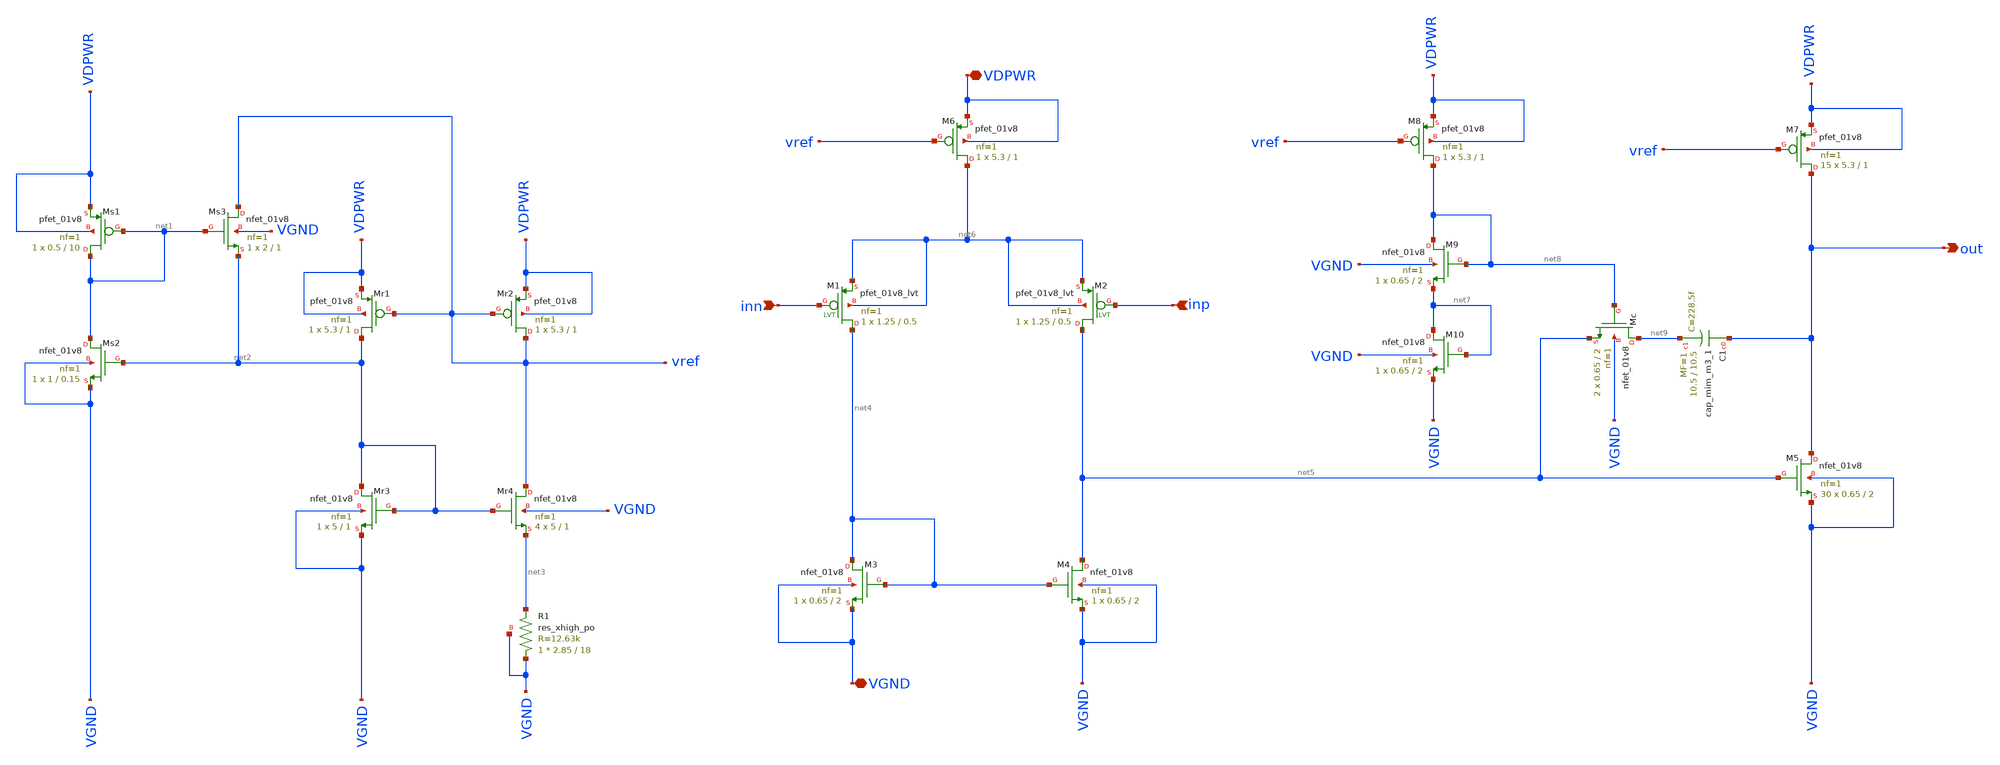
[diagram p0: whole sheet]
** sch_path: src/xschem/miller_ota.sch
**.subckt miller_ota inp out inn VDPWR VGND
*.ipin inp
*.opin out
*.ipin inn
*.iopin VDPWR
*.iopin VGND
XMs1 net1 net1 VDPWR VDPWR sky130_fd_pr__pfet_01v8 L=10 W=0.5 nf=1 ad='int((1 + 1)/2) * 0.5 / 1 * 0.29'
+ as='int((1 + 2)/2) * 0.5 / 1 * 0.29' pd='2*int((1 + 1)/2) * (0.5 / 1 + 0.29)' ps='2*int((1 + 2)/2) * (0.5 / 1 + 0.29)'
+ nrd='0.29 / 0.5 ' nrs='0.29 / 0.5 ' sa=0 sb=0 sd=0 mult=1 m=1
XMs3 vref net1 net2 VGND sky130_fd_pr__nfet_01v8 L=1 W=2 nf=1 ad='int((1 + 1)/2) * 2 / 1 * 0.29' as='int((1 + 2)/2) * 2 / 1 * 0.29'
+ pd='2*int((1 + 1)/2) * (2 / 1 + 0.29)' ps='2*int((1 + 2)/2) * (2 / 1 + 0.29)' nrd='0.29 / 2 ' nrs='0.29 / 2 '
+ sa=0 sb=0 sd=0 mult=1 m=1
XMs2 net1 net2 VGND VGND sky130_fd_pr__nfet_01v8 L=0.15 W=1 nf=1 ad='int((1 + 1)/2) * 1 / 1 * 0.29' as='int((1 + 2)/2) * 1 / 1 * 0.29'
+ pd='2*int((1 + 1)/2) * (1 / 1 + 0.29)' ps='2*int((1 + 2)/2) * (1 / 1 + 0.29)' nrd='0.29 / 1 ' nrs='0.29 / 1 '
+ sa=0 sb=0 sd=0 mult=1 m=1
XMr3 net2 net2 VGND VGND sky130_fd_pr__nfet_01v8 L=1 W=5 nf=1 ad='int((1 + 1)/2) * 5 / 1 * 0.29' as='int((1 + 2)/2) * 5 / 1 * 0.29'
+ pd='2*int((1 + 1)/2) * (5 / 1 + 0.29)' ps='2*int((1 + 2)/2) * (5 / 1 + 0.29)' nrd='0.29 / 5 ' nrs='0.29 / 5 '
+ sa=0 sb=0 sd=0 mult=1 m=1
XMr1 net2 vref VDPWR VDPWR sky130_fd_pr__pfet_01v8 L=1 W=5.3 nf=1 ad='int((1 + 1)/2) * 5.3 / 1 * 0.29'
+ as='int((1 + 2)/2) * 5.3 / 1 * 0.29' pd='2*int((1 + 1)/2) * (5.3 / 1 + 0.29)' ps='2*int((1 + 2)/2) * (5.3 / 1 + 0.29)'
+ nrd='0.29 / 5.3 ' nrs='0.29 / 5.3 ' sa=0 sb=0 sd=0 mult=1 m=1
XMr2 vref vref VDPWR VDPWR sky130_fd_pr__pfet_01v8 L=1 W=5.3 nf=1 ad='int((1 + 1)/2) * 5.3 / 1 * 0.29'
+ as='int((1 + 2)/2) * 5.3 / 1 * 0.29' pd='2*int((1 + 1)/2) * (5.3 / 1 + 0.29)' ps='2*int((1 + 2)/2) * (5.3 / 1 + 0.29)'
+ nrd='0.29 / 5.3 ' nrs='0.29 / 5.3 ' sa=0 sb=0 sd=0 mult=1 m=1
XMr4 vref net2 net3 VGND sky130_fd_pr__nfet_01v8 L=1 W=5 nf=1 ad='int((1 + 1)/2) * 5 / 1 * 0.29' as='int((1 + 2)/2) * 5 / 1 * 0.29'
+ pd='2*int((1 + 1)/2) * (5 / 1 + 0.29)' ps='2*int((1 + 2)/2) * (5 / 1 + 0.29)' nrd='0.29 / 5 ' nrs='0.29 / 5 '
+ sa=0 sb=0 sd=0 mult=4 m=4
XR1 VGND net3 VGND sky130_fd_pr__res_xhigh_po W=2.85 L=18 mult=1 m=1
XM4 net5 net4 VGND VGND sky130_fd_pr__nfet_01v8 L=2 W=0.65 nf=1 ad='int((1 + 1)/2) * 0.65 / 1 * 0.29'
+ as='int((1 + 2)/2) * 0.65 / 1 * 0.29' pd='2*int((1 + 1)/2) * (0.65 / 1 + 0.29)' ps='2*int((1 + 2)/2) * (0.65 / 1 + 0.29)'
+ nrd='0.29 / 0.65 ' nrs='0.29 / 0.65 ' sa=0 sb=0 sd=0 mult=1 m=1
XM3 net4 net4 VGND VGND sky130_fd_pr__nfet_01v8 L=2 W=0.65 nf=1 ad='int((1 + 1)/2) * 0.65 / 1 * 0.29'
+ as='int((1 + 2)/2) * 0.65 / 1 * 0.29' pd='2*int((1 + 1)/2) * (0.65 / 1 + 0.29)' ps='2*int((1 + 2)/2) * (0.65 / 1 + 0.29)'
+ nrd='0.29 / 0.65 ' nrs='0.29 / 0.65 ' sa=0 sb=0 sd=0 mult=1 m=1
XM1 net4 inn net6 net6 sky130_fd_pr__pfet_01v8_lvt L=0.5 W=1.25 nf=1 ad='int((1 + 1)/2) * 1.25 / 1 * 0.29'
+ as='int((1 + 2)/2) * 1.25 / 1 * 0.29' pd='2*int((1 + 1)/2) * (1.25 / 1 + 0.29)' ps='2*int((1 + 2)/2) * (1.25 / 1 + 0.29)'
+ nrd='0.29 / 1.25 ' nrs='0.29 / 1.25 ' sa=0 sb=0 sd=0 mult=1 m=1
XM2 net5 inp net6 net6 sky130_fd_pr__pfet_01v8_lvt L=0.5 W=1.25 nf=1 ad='int((1 + 1)/2) * 1.25 / 1 * 0.29'
+ as='int((1 + 2)/2) * 1.25 / 1 * 0.29' pd='2*int((1 + 1)/2) * (1.25 / 1 + 0.29)' ps='2*int((1 + 2)/2) * (1.25 / 1 + 0.29)'
+ nrd='0.29 / 1.25 ' nrs='0.29 / 1.25 ' sa=0 sb=0 sd=0 mult=1 m=1
XM9 net8 net8 net7 VGND sky130_fd_pr__nfet_01v8 L=2 W=0.65 nf=1 ad='int((1 + 1)/2) * 0.65 / 1 * 0.29'
+ as='int((1 + 2)/2) * 0.65 / 1 * 0.29' pd='2*int((1 + 1)/2) * (0.65 / 1 + 0.29)' ps='2*int((1 + 2)/2) * (0.65 / 1 + 0.29)'
+ nrd='0.29 / 0.65 ' nrs='0.29 / 0.65 ' sa=0 sb=0 sd=0 mult=1 m=1
XM10 net7 net7 VGND VGND sky130_fd_pr__nfet_01v8 L=2 W=0.65 nf=1 ad='int((1 + 1)/2) * 0.65 / 1 * 0.29'
+ as='int((1 + 2)/2) * 0.65 / 1 * 0.29' pd='2*int((1 + 1)/2) * (0.65 / 1 + 0.29)' ps='2*int((1 + 2)/2) * (0.65 / 1 + 0.29)'
+ nrd='0.29 / 0.65 ' nrs='0.29 / 0.65 ' sa=0 sb=0 sd=0 mult=1 m=1
XMc net9 net8 net5 VGND sky130_fd_pr__nfet_01v8 L=2 W=0.65 nf=1 ad='int((1 + 1)/2) * 0.65 / 1 * 0.29'
+ as='int((1 + 2)/2) * 0.65 / 1 * 0.29' pd='2*int((1 + 1)/2) * (0.65 / 1 + 0.29)' ps='2*int((1 + 2)/2) * (0.65 / 1 + 0.29)'
+ nrd='0.29 / 0.65 ' nrs='0.29 / 0.65 ' sa=0 sb=0 sd=0 mult=2 m=2
XC1 out net9 sky130_fd_pr__cap_mim_m3_1 W=10.5 L=10.5 MF=1 m=1
XM5 out net5 VGND VGND sky130_fd_pr__nfet_01v8 L=2 W=0.65 nf=1 ad='int((1 + 1)/2) * 0.65 / 1 * 0.29'
+ as='int((1 + 2)/2) * 0.65 / 1 * 0.29' pd='2*int((1 + 1)/2) * (0.65 / 1 + 0.29)' ps='2*int((1 + 2)/2) * (0.65 / 1 + 0.29)'
+ nrd='0.29 / 0.65 ' nrs='0.29 / 0.65 ' sa=0 sb=0 sd=0 mult=30 m=30
XM8 net8 vref VDPWR VDPWR sky130_fd_pr__pfet_01v8 L=1 W=5.3 nf=1 ad='int((1 + 1)/2) * 5.3 / 1 * 0.29'
+ as='int((1 + 2)/2) * 5.3 / 1 * 0.29' pd='2*int((1 + 1)/2) * (5.3 / 1 + 0.29)' ps='2*int((1 + 2)/2) * (5.3 / 1 + 0.29)'
+ nrd='0.29 / 5.3 ' nrs='0.29 / 5.3 ' sa=0 sb=0 sd=0 mult=1 m=1
XM7 out vref VDPWR VDPWR sky130_fd_pr__pfet_01v8 L=1 W=5.3 nf=1 ad='int((1 + 1)/2) * 5.3 / 1 * 0.29'
+ as='int((1 + 2)/2) * 5.3 / 1 * 0.29' pd='2*int((1 + 1)/2) * (5.3 / 1 + 0.29)' ps='2*int((1 + 2)/2) * (5.3 / 1 + 0.29)'
+ nrd='0.29 / 5.3 ' nrs='0.29 / 5.3 ' sa=0 sb=0 sd=0 mult=15 m=15
XM6 net6 vref VDPWR VDPWR sky130_fd_pr__pfet_01v8 L=1 W=5.3 nf=1 ad='int((1 + 1)/2) * 5.3 / 1 * 0.29'
+ as='int((1 + 2)/2) * 5.3 / 1 * 0.29' pd='2*int((1 + 1)/2) * (5.3 / 1 + 0.29)' ps='2*int((1 + 2)/2) * (5.3 / 1 + 0.29)'
+ nrd='0.29 / 5.3 ' nrs='0.29 / 5.3 ' sa=0 sb=0 sd=0 mult=1 m=1
**.ends
.end
